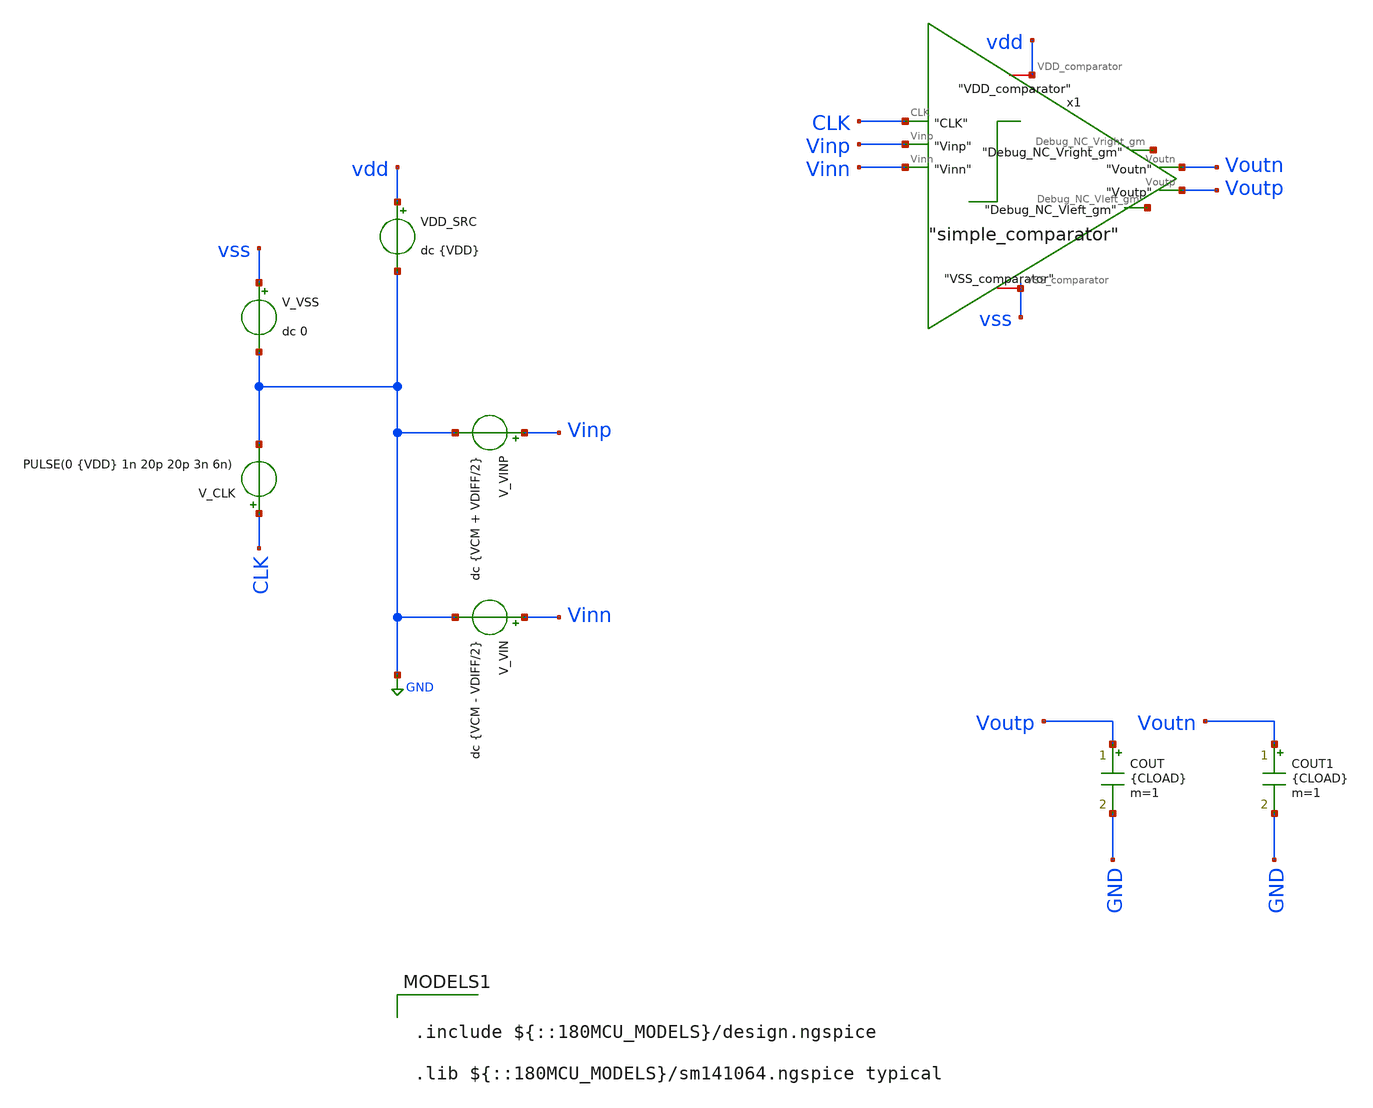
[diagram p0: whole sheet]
** sch_path: circuit_files/xschem_symbols/untitled.sch
**.subckt untitled
V_VIN Vinn GND dc {VCM - VDIFF/2}
VDD_SRC vdd GND dc {VDD}
V_VINP Vinp GND dc {VCM + VDIFF/2}
V_VSS vss GND dc 0
V_CLK CLK GND PULSE(0 {VDD} 1n 20p 20p 3n 6n)
COUT Voutp GND {CLOAD} m=1
COUT1 Voutn GND {CLOAD} m=1
x1 vdd CLK Voutn Voutp net1 net2 Vinp Vinn vss simple_comparator
**** begin user architecture code



.param VDD=3.3
.param VCM=1.65
.param VREF=3.3
.param NBITS=10
.param VLSB=3.22265625e-3
.param VHLSB=1.611328125e-3
.param VDIFF=10e-3
.param CLOAD=20f

.options savecurrents
.options reltol=1e-4 abstol=1e-12 vntol=1e-6 method=gear

.save v(CLK) v(Vinp) v(Vinn) v(Voutp) v(Voutn)
.save v(x1.x) v(x1.y) v(x1.p) v(x1.q) v(x1.net1) v(x1.net2) v(x1.net3)
.save i(VDD_SRC)

.control
set filetype=binary

shell rm -f strongarm_results.txt
shell rm -f strongarm_tran_nominal.txt
shell rm -f strongarm_lsb_sweep.txt
shell rm -f strongarm_delay_sweep.txt
shell rm -f strongarm_vcm_sweep.txt
shell rm -f strongarm_vdd_sweep.txt

echo ============================================= > strongarm_results.txt
echo GF180MCU StrongARM comparator qualification >> strongarm_results.txt
echo For 10-bit SAR ADC check >> strongarm_results.txt
echo ============================================= >> strongarm_results.txt
echo . >> strongarm_results.txt
echo Assumed VREF = 3.3 V >> strongarm_results.txt
echo 10-bit LSB  = 3.22265625 mV >> strongarm_results.txt
echo 0.5 LSB     = 1.611328125 mV >> strongarm_results.txt
echo . >> strongarm_results.txt

****************************************************
* 1. Nominal transient at VDIFF = +10 mV
****************************************************

alterparam VDD=3.3
alterparam VCM=1.65
alterparam VDIFF=10e-3
reset

op
tran 1p 5n
write strong_arm_comp_tb.raw

meas tran voutp_samp FIND v(Voutp) AT=4n
meas tran voutn_samp FIND v(Voutn) AT=4n
meas tran x_samp     FIND v(x1.x)     AT=4n
meas tran y_samp     FIND v(x1.y)     AT=4n
meas tran p_samp     FIND v(x1.p)     AT=4n
meas tran q_samp     FIND v(x1.q)     AT=4n
meas tran net1_samp  FIND v(x1.net1)  AT=4n
meas tran net2_samp  FIND v(x1.net2)  AT=4n
meas tran net3_samp  FIND v(x1.net3)  AT=4n

meas tran idd_avg    AVG i(VDD_SRC) FROM=0n TO=5n
meas tran idd_eval   AVG i(VDD_SRC) FROM=1n TO=4n

let vod_samp = voutp_samp - voutn_samp
let pavg = -3.3*idd_avg
let peval = -3.3*idd_eval
let e_5ns = pavg*5n
let e_eval = peval*3n

meas tran t_clk_rise WHEN v(CLK)=1.65 RISE=1
meas tran t_voutn_fall WHEN v(Voutn)=1.65 FALL=1
let td_pos = t_voutn_fall - t_clk_rise

echo ---- Nominal transient result, VDIFF = +10 mV ---- >> strongarm_results.txt
echo Voutp_4ns          = $&voutp_samp V >> strongarm_results.txt
echo Voutn_4ns          = $&voutn_samp V >> strongarm_results.txt
echo Voutp_minus_Voutn  = $&vod_samp   V >> strongarm_results.txt
echo X_4ns              = $&x_samp     V >> strongarm_results.txt
echo Y_4ns              = $&y_samp     V >> strongarm_results.txt
echo P_4ns              = $&p_samp     V >> strongarm_results.txt
echo Q_4ns              = $&q_samp     V >> strongarm_results.txt
echo net1_4ns           = $&net1_samp  V >> strongarm_results.txt
echo net2_4ns           = $&net2_samp  V >> strongarm_results.txt
echo net3_4ns           = $&net3_samp  V >> strongarm_results.txt
echo IDD_avg_0_to_5ns   = $&idd_avg    A >> strongarm_results.txt
echo Pavg_0_to_5ns      = $&pavg       W >> strongarm_results.txt
echo E_0_to_5ns         = $&e_5ns      J >> strongarm_results.txt
echo IDD_eval_1_to_4ns  = $&idd_eval   A >> strongarm_results.txt
echo Peval_1_to_4ns     = $&peval      W >> strongarm_results.txt
echo Eeval_1_to_4ns     = $&e_eval     J >> strongarm_results.txt
echo t_clk_rise         = $&t_clk_rise     s >> strongarm_results.txt
echo t_voutn_fall       = $&t_voutn_fall   s >> strongarm_results.txt
echo td_pos             = $&td_pos         s >> strongarm_results.txt
echo . >> strongarm_results.txt

wrdata strongarm_tran_nominal.txt time v(CLK) v(Vinp) v(Vinn) v(Voutp) v(Voutn) v(x1.x) v(x1.y)
+ v(x1.p) v(x1.q) v(x1.net1) v(x1.net2) v(x1.net3) i(VDD_SRC)
****************************************************
* 2. 10-bit LSB decision sweep
****************************************************

echo ============================================= > strongarm_lsb_sweep.txt
echo 10-bit SAR LSB decision sweep >> strongarm_lsb_sweep.txt
echo VREF = 3.3 V, LSB = 3.22265625 mV, 0.5LSB = 1.611328125 mV >> strongarm_lsb_sweep.txt
echo columns: VDIFF Voutp Voutn Vod X Y P Q net1 net2 net3 Pavg >> strongarm_lsb_sweep.txt
echo ============================================= >> strongarm_lsb_sweep.txt

foreach dv -10e-3 -5e-3 -3.22265625e-3 -1.611328125e-3 -1e-3 -500e-6 500e-6 1e-3 1.611328125e-3
+ 3.22265625e-3 5e-3 10e-3
  alterparam VDD=3.3
  alterparam VCM=1.65
  alterparam VDIFF=$dv
  reset
  tran 1p 5n

  meas tran vop FIND v(Voutp) AT=4n
  meas tran von FIND v(Voutn) AT=4n
  meas tran vx  FIND v(x1.x)     AT=4n
meas tran vy  FIND v(x1.y)     AT=4n
meas tran vp  FIND v(x1.p)     AT=4n
meas tran vq  FIND v(x1.q)     AT=4n
meas tran vn1 FIND v(x1.net1)  AT=4n
meas tran vn2 FIND v(x1.net2)  AT=4n
meas tran vn3 FIND v(x1.net3)  AT=4n
  meas tran ia  AVG i(VDD_SRC) FROM=0n TO=5n

  let vod = vop - von
  let ppwr = -3.3*ia

  echo $dv $&vop $&von $&vod $&vx $&vy $&vp $&vq $&vn1 $&vn2 $&vn3 $&ppwr >> strongarm_lsb_sweep.txt
end

****************************************************
* 3. Delay versus positive VDIFF
****************************************************

echo ============================================= > strongarm_delay_sweep.txt
echo Delay versus positive VDIFF >> strongarm_delay_sweep.txt
echo columns: VDIFF tclk tout td Voutp4n Voutn4n Pavg >> strongarm_delay_sweep.txt
echo ============================================= >> strongarm_delay_sweep.txt

foreach dv 500e-6 1e-3 1.611328125e-3 3.22265625e-3 5e-3 10e-3 20e-3 50e-3
  alterparam VDD=3.3
  alterparam VCM=1.65
  alterparam VDIFF=$dv
  reset
  tran 1p 5n

  meas tran tclk WHEN v(CLK)=1.65 RISE=1
  meas tran tout WHEN v(Voutn)=1.65 FALL=1
  let td = tout - tclk

  meas tran vop4 FIND v(Voutp) AT=4n
  meas tran von4 FIND v(Voutn) AT=4n
  meas tran ia AVG i(VDD_SRC) FROM=0n TO=5n
  let ppwr = -3.3*ia

  echo $dv $&tclk $&tout $&td $&vop4 $&von4 $&ppwr >> strongarm_delay_sweep.txt
end

****************************************************
* 4. Input common-mode sweep at +0.5 LSB
****************************************************

echo ============================================= > strongarm_vcm_sweep.txt
echo VCM sweep at VDIFF = +0.5 LSB >> strongarm_vcm_sweep.txt
echo columns: VCM Voutp4n Voutn4n Vod4n td Pavg >> strongarm_vcm_sweep.txt
echo ============================================= >> strongarm_vcm_sweep.txt

foreach cm 0.8 1.0 1.2 1.4 1.65 1.8 2.0 2.2 2.4
  alterparam VDD=3.3
  alterparam VCM=$cm
  alterparam VDIFF=1.611328125e-3
  reset
  tran 1p 5n

  meas tran vop4 FIND v(Voutp) AT=4n
  meas tran von4 FIND v(Voutn) AT=4n
  let vod4 = vop4 - von4

  meas tran tclk WHEN v(CLK)=1.65 RISE=1
  meas tran tout WHEN v(Voutn)=1.65 FALL=1
  let td = tout - tclk

  meas tran ia AVG i(VDD_SRC) FROM=0n TO=5n
  let ppwr = -3.3*ia

  echo $cm $&vop4 $&von4 $&vod4 $&td $&ppwr >> strongarm_vcm_sweep.txt
end

****************************************************
* 5. Supply sweep at +0.5 LSB
****************************************************

echo ============================================= > strongarm_vdd_sweep.txt
echo VDD sweep at VCM=VDD/2 and VDIFF=+0.5LSB >> strongarm_vdd_sweep.txt
echo columns: VDD VCM Voutp4n Voutn4n Vod4n td Pavg >> strongarm_vdd_sweep.txt
echo ============================================= >> strongarm_vdd_sweep.txt

* VDD = 3.0 V, VCM = 1.5 V
alterparam VDD=3.0
alterparam VCM=1.5
alterparam VDIFF=1.611328125e-3
reset
tran 1p 5n
meas tran vop4 FIND v(Voutp) AT=4n
meas tran von4 FIND v(Voutn) AT=4n
let vod4 = vop4 - von4
meas tran tclk WHEN v(CLK)=1.5 RISE=1
meas tran tout WHEN v(Voutn)=1.5 FALL=1
let td = tout - tclk
meas tran ia AVG i(VDD_SRC) FROM=0n TO=5n
let ppwr = -3.0*ia
echo 3.0 1.5 $&vop4 $&von4 $&vod4 $&td $&ppwr >> strongarm_vdd_sweep.txt

* VDD = 3.15 V, VCM = 1.575 V
alterparam VDD=3.15
alterparam VCM=1.575
alterparam VDIFF=1.611328125e-3
reset
tran 1p 5n
meas tran vop4 FIND v(Voutp) AT=4n
meas tran von4 FIND v(Voutn) AT=4n
let vod4 = vop4 - von4
meas tran tclk WHEN v(CLK)=1.575 RISE=1
meas tran tout WHEN v(Voutn)=1.575 FALL=1
let td = tout - tclk
meas tran ia AVG i(VDD_SRC) FROM=0n TO=5n
let ppwr = -3.15*ia
echo 3.15 1.575 $&vop4 $&von4 $&vod4 $&td $&ppwr >> strongarm_vdd_sweep.txt

* VDD = 3.3 V, VCM = 1.65 V
alterparam VDD=3.3
alterparam VCM=1.65
alterparam VDIFF=1.611328125e-3
reset
tran 1p 5n
meas tran vop4 FIND v(Voutp) AT=4n
meas tran von4 FIND v(Voutn) AT=4n
let vod4 = vop4 - von4
meas tran tclk WHEN v(CLK)=1.65 RISE=1
meas tran tout WHEN v(Voutn)=1.65 FALL=1
let td = tout - tclk
meas tran ia AVG i(VDD_SRC) FROM=0n TO=5n
let ppwr = -3.3*ia
echo 3.3 1.65 $&vop4 $&von4 $&vod4 $&td $&ppwr >> strongarm_vdd_sweep.txt

* VDD = 3.45 V, VCM = 1.725 V
alterparam VDD=3.45
alterparam VCM=1.725
alterparam VDIFF=1.611328125e-3
reset
tran 1p 5n
meas tran vop4 FIND v(Voutp) AT=4n
meas tran von4 FIND v(Voutn) AT=4n
let vod4 = vop4 - von4
meas tran tclk WHEN v(CLK)=1.725 RISE=1
meas tran tout WHEN v(Voutn)=1.725 FALL=1
let td = tout - tclk
meas tran ia AVG i(VDD_SRC) FROM=0n TO=5n
let ppwr = -3.45*ia
echo 3.45 1.725 $&vop4 $&von4 $&vod4 $&td $&ppwr >> strongarm_vdd_sweep.txt

* VDD = 3.6 V, VCM = 1.8 V
alterparam VDD=3.6
alterparam VCM=1.8
alterparam VDIFF=1.611328125e-3
reset
tran 1p 5n
meas tran vop4 FIND v(Voutp) AT=4n
meas tran von4 FIND v(Voutn) AT=4n
let vod4 = vop4 - von4
meas tran tclk WHEN v(CLK)=1.8 RISE=1
meas tran tout WHEN v(Voutn)=1.8 FALL=1
let td = tout - tclk
meas tran ia AVG i(VDD_SRC) FROM=0n TO=5n
let ppwr = -3.6*ia
echo 3.6 1.8 $&vop4 $&von4 $&vod4 $&td $&ppwr >> strongarm_vdd_sweep.txt

echo . >> strongarm_results.txt
echo Additional files generated: >> strongarm_results.txt
echo strongarm_lsb_sweep.txt >> strongarm_results.txt
echo strongarm_delay_sweep.txt >> strongarm_results.txt
echo strongarm_vcm_sweep.txt >> strongarm_results.txt
echo strongarm_vdd_sweep.txt >> strongarm_results.txt

echo Simulation complete.

.endc




.include ${::180MCU_MODELS}/design.ngspice

.lib ${::180MCU_MODELS}/sm141064.ngspice typical


**** end user architecture code
**.ends

* expanding   symbol:  simple_comparator.sym # of pins=9
** sym_path: circuit_files/xschem_symbols/simple_comparator.sym
** sch_path: circuit_files/xschem_symbols/simple_comparator.sch
.subckt simple_comparator VDD_comparator CLK Voutn Voutp Debug_NC_Vright_gm Debug_NC_Vleft_gm Vinp
+ Vinn VSS_comparator
*.ipin CLK
*.ipin Vinp
*.iopin VSS_comparator
*.iopin VDD_comparator
*.ipin Vinn
*.opin Debug_NC_Vright_gm
*.opin Debug_NC_Vleft_gm
*.opin Voutp
*.opin Voutn
XM1 net2 net1 VDD_comparator VDD_comparator sg13_hv_pmos w=0.3u l=0.4u ng=1 m=1 mm_ok=1
XM2 Debug_NC_Vleft_gm Vinp VS_dp VSS_comparator sg13_hv_nmos w=0.3u l=0.45u ng=1 m=1 mm_ok=1
XM3 net2 net1 Debug_NC_Vleft_gm VSS_comparator sg13_hv_nmos w=0.3u l=0.45u ng=1 m=1 mm_ok=1
XM4 Debug_NC_Vright_gm Vinn VS_dp VSS_comparator sg13_hv_nmos w=0.3u l=0.45u ng=1 m=1 mm_ok=1
XM5 net1 net2 Debug_NC_Vright_gm VSS_comparator sg13_hv_nmos w=0.3u l=0.45u ng=1 m=1 mm_ok=1
XM6 net1 net2 VDD_comparator VDD_comparator sg13_hv_pmos w=0.3u l=0.4u ng=1 m=1 mm_ok=1
XM7 VS_dp CLK VSS_comparator VSS_comparator sg13_hv_nmos w=0.3u l=0.45u ng=1 m=1 mm_ok=1
XM8 net1 CLK VDD_comparator VDD_comparator sg13_hv_pmos w=0.3u l=0.4u ng=1 m=1 mm_ok=1
XM9 net2 CLK VDD_comparator VDD_comparator sg13_hv_pmos w=0.3u l=0.4u ng=1 m=1 mm_ok=1
XM10 net3 net1 VDD_comparator VDD_comparator sg13_hv_pmos w=0.3u l=0.4u ng=1 m=1 mm_ok=1
XM11 net3 net1 VSS_comparator VSS_comparator sg13_hv_nmos w=0.3u l=0.45u ng=1 m=1 mm_ok=1
XM12 Voutn net3 VDD_comparator VDD_comparator sg13_hv_pmos w=0.3u l=0.4u ng=1 m=1 mm_ok=1
XM13 Voutn net3 VSS_comparator VSS_comparator sg13_hv_nmos w=0.3u l=0.45u ng=1 m=1 mm_ok=1
XM14 VDD_comparator net2 VDD_comparator VDD_comparator sg13_hv_pmos w=0.3u l=0.4u ng=1 m=1 mm_ok=1
XM15 VDD_comparator net2 VSS_comparator VSS_comparator sg13_hv_nmos w=0.3u l=0.45u ng=1 m=1 mm_ok=1
XM16 Voutp VDD_comparator VDD_comparator VDD_comparator sg13_hv_pmos w=0.3u l=0.4u ng=1 m=1 mm_ok=1
XM17 Voutp VDD_comparator VSS_comparator VSS_comparator sg13_hv_nmos w=0.3u l=0.45u ng=1 m=1 mm_ok=1
.ends

.GLOBAL GND
.end
